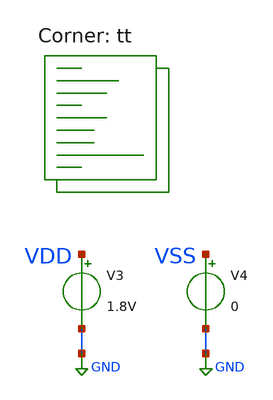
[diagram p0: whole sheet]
** sch_path: xschem/tests/default_template_test.sch
**.subckt default_template_test
V3 VDD GND 1.8V
V4 VSS GND 0
**** begin user architecture code
 *.lib $::SKYWATER_MODELS/sky130.lib.spice tt
.include $::SKYWATER_STDCELLS/sky130_fd_sc_hd.spice


.options acct list
.temp 25
*vvcc VDD 0 dc 1.8
*vvss VSS 0 0
.control
tran 0.1u 400u
*plot RST_PLS clk+2 Pulse+4
write pulse_generator_test.raw
.endc


.lib $::SKYWATER_MODELS/sky130.lib.spice tt
**** end user architecture code
**.ends
.GLOBAL GND
.end
